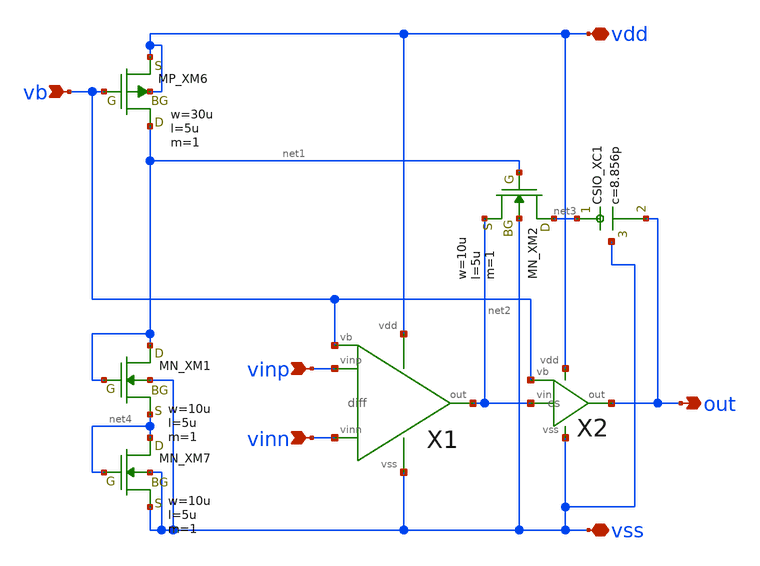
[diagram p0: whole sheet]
** sch_path: member_project/OPAMP/kano/sch_tb/2stage_pc.sch
**.subckt 2stage_pc vinp vinn vb out vdd vss
*.ipin vinp
*.ipin vinn
*.ipin vb
*.opin out
*.iopin vdd
*.iopin vss
X1 vinp vinn net2 vdd vss vb diff
X2 net2 vb out vdd vss cs
XM6 net1 vb vdd vdd PMOS w=30u l=5u as=0 ad=0 ps=0 pd=0 nrd=0 nrs=0 m=1
XM1 net1 net1 net4 vss NMOS w=10u l=5u as=0 ad=0 ps=0 pd=0 nrd=0 nrs=0 m=1
XM7 net4 net4 vss vss NMOS w=10u l=5u as=0 ad=0 ps=0 pd=0 nrd=0 nrs=0 m=1
XM2 net3 net1 net2 vss NMOS w=10u l=5u as=0 ad=0 ps=0 pd=0 nrd=0 nrs=0 m=1
XC1 net3 out vss F_CSIO c=8.856p x=120u y=120u m=1
**.ends

* expanding   symbol:  diff.sym # of pins=6
** sym_path: diff.sym
** sch_path: diff.sch
.subckt diff vinp vinn out vdd vss vb
*.ipin vinn
*.ipin vinp
*.ipin vb
*.opin out
*.iopin vdd
*.iopin vss
XM5 net2 vb vdd vdd PMOS w=720u l=5u as=0 ad=0 ps=0 pd=0 nrd=0 nrs=0 m=1
XM1 net1 vinn net2 net2 PMOS w=1080u l=5u as=0 ad=0 ps=0 pd=0 nrd=0 nrs=0 m=1
XM2 out vinp net2 net2 PMOS w=1080u l=5u as=0 ad=0 ps=0 pd=0 nrd=0 nrs=0 m=1
XM3 net1 net1 vss vss NMOS w=120u l=5u as=0 ad=0 ps=0 pd=0 nrd=0 nrs=0 m=1
XM4 out net1 vss vss NMOS w=120u l=5u as=0 ad=0 ps=0 pd=0 nrd=0 nrs=0 m=1
.ends


* expanding   symbol:  cs.sym # of pins=5
** sym_path: cs.sym
** sch_path: cs.sch
.subckt cs vin vb out vdd vss
*.ipin vb
*.ipin vin
*.opin out
*.iopin vss
*.iopin vdd
XM6 out vb vdd vdd PMOS w=600u l=5u as=0 ad=0 ps=0 pd=0 nrd=0 nrs=0 m=1
XM7 out vin vss vss NMOS w=200u l=5u as=0 ad=0 ps=0 pd=0 nrd=0 nrs=0 m=1
.ends

.end
